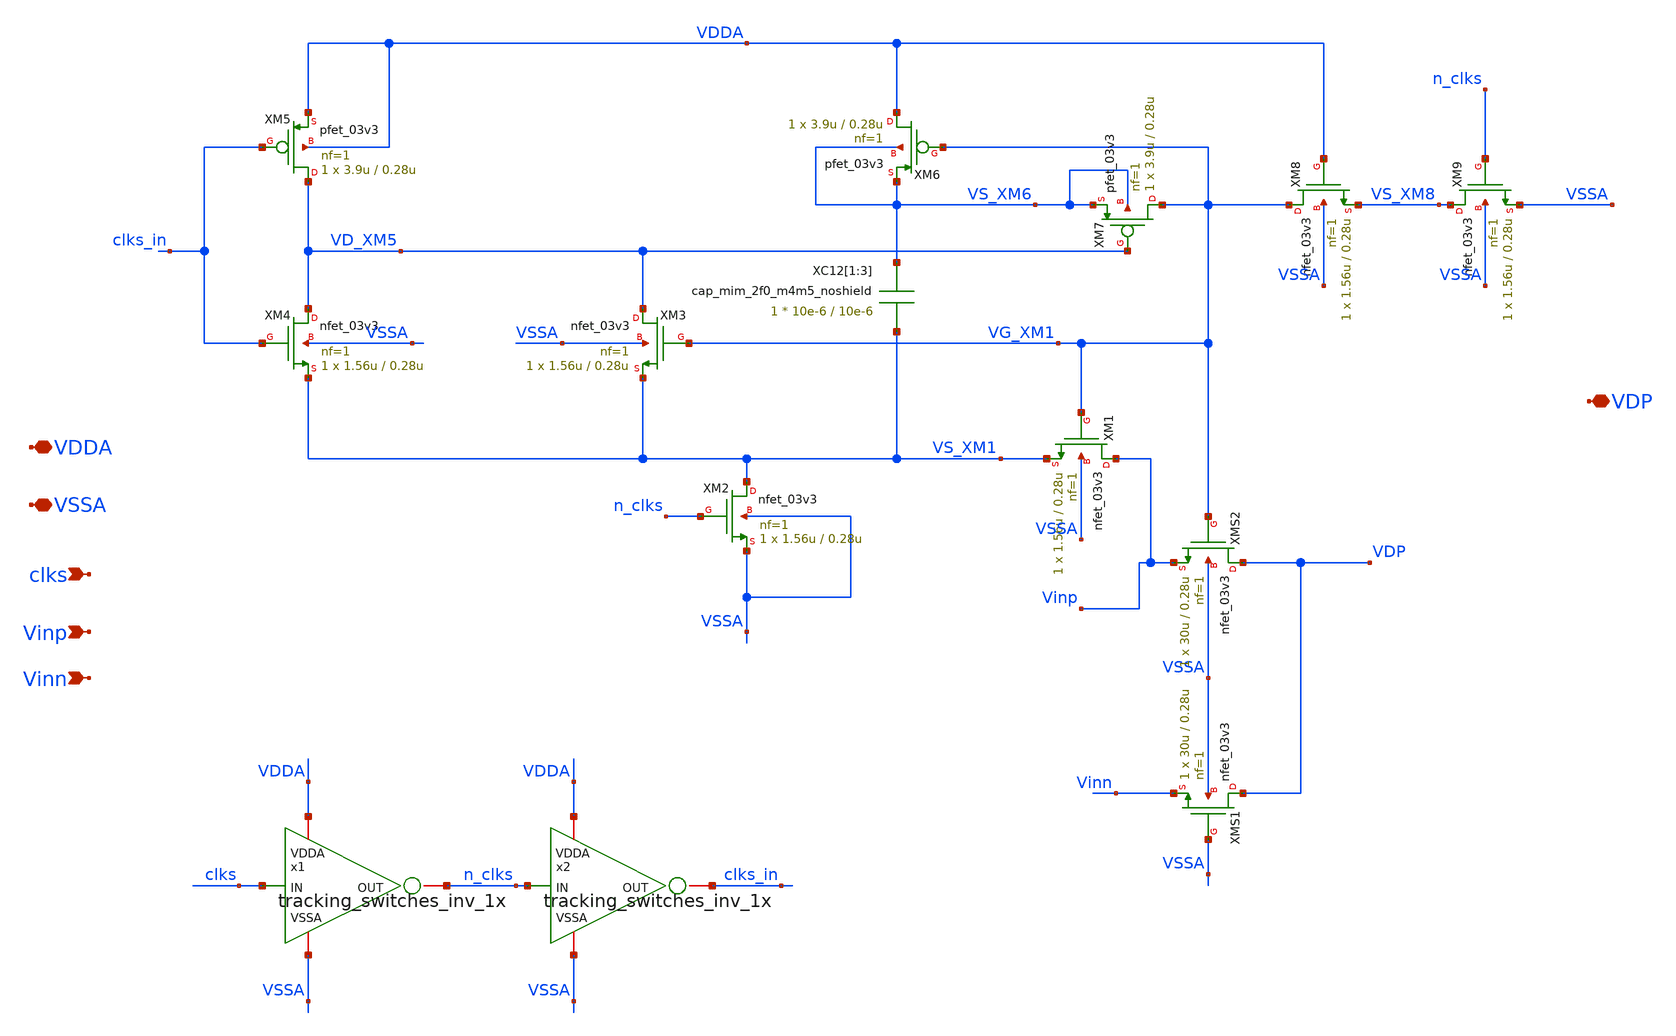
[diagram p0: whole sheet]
** sch_path: SAR_ADC/tracking_switches/xschem/tracking_switches_v1.sch
**.subckt tracking_switches_v1 VDDA VSSA clks Vinp VDP Vinn
*.iopin VDDA
*.iopin VSSA
*.ipin clks
*.ipin Vinp
*.iopin VDP
*.ipin Vinn
XM2 VS_XM1 n_clks VSSA VSSA nfet_03v3 L=0.28u W=1.56u nf=1 ad='int((nf+1)/2) * W/nf * 0.18u' as='int((nf+2)/2) * W/nf * 0.18u'
+ pd='2*int((nf+1)/2) * (W/nf + 0.18u)' ps='2*int((nf+2)/2) * (W/nf + 0.18u)' nrd='0.18u / W' nrs='0.18u / W'
+ sa=0 sb=0 sd=0 m=1
XM4 VD_XM5 clks_in VS_XM1 VSSA nfet_03v3 L=0.28u W=1.56u nf=1 ad='int((nf+1)/2) * W/nf * 0.18u' as='int((nf+2)/2) * W/nf * 0.18u'
+ pd='2*int((nf+1)/2) * (W/nf + 0.18u)' ps='2*int((nf+2)/2) * (W/nf + 0.18u)' nrd='0.18u / W' nrs='0.18u / W'
+ sa=0 sb=0 sd=0 m=1
XM3 VD_XM5 VG_XM1 VS_XM1 VSSA nfet_03v3 L=0.28u W=1.56u nf=1 ad='int((nf+1)/2) * W/nf * 0.18u' as='int((nf+2)/2) * W/nf * 0.18u'
+ pd='2*int((nf+1)/2) * (W/nf + 0.18u)' ps='2*int((nf+2)/2) * (W/nf + 0.18u)' nrd='0.18u / W' nrs='0.18u / W'
+ sa=0 sb=0 sd=0 m=1
XM5 VD_XM5 clks_in VDDA VDDA pfet_03v3 L=0.28u W=3.9u nf=1 ad='int((nf+1)/2) * W/nf * 0.18u' as='int((nf+2)/2) * W/nf * 0.18u'
+ pd='2*int((nf+1)/2) * (W/nf + 0.18u)' ps='2*int((nf+2)/2) * (W/nf + 0.18u)' nrd='0.18u / W' nrs='0.18u / W'
+ sa=0 sb=0 sd=0 m=1
XM6 VDDA VG_XM1 VS_XM6 VS_XM6 pfet_03v3 L=0.28u W=3.9u nf=1 ad='int((nf+1)/2) * W/nf * 0.18u' as='int((nf+2)/2) * W/nf * 0.18u'
+ pd='2*int((nf+1)/2) * (W/nf + 0.18u)' ps='2*int((nf+2)/2) * (W/nf + 0.18u)' nrd='0.18u / W' nrs='0.18u / W'
+ sa=0 sb=0 sd=0 m=1
XM7 VG_XM1 VD_XM5 VS_XM6 VS_XM6 pfet_03v3 L=0.28u W=3.9u nf=1 ad='int((nf+1)/2) * W/nf * 0.18u' as='int((nf+2)/2) * W/nf * 0.18u'
+ pd='2*int((nf+1)/2) * (W/nf + 0.18u)' ps='2*int((nf+2)/2) * (W/nf + 0.18u)' nrd='0.18u / W' nrs='0.18u / W'
+ sa=0 sb=0 sd=0 m=1
XM1 Vinp VG_XM1 VS_XM1 VSSA nfet_03v3 L=0.28u W=1.56u nf=1 ad='int((nf+1)/2) * W/nf * 0.18u' as='int((nf+2)/2) * W/nf * 0.18u'
+ pd='2*int((nf+1)/2) * (W/nf + 0.18u)' ps='2*int((nf+2)/2) * (W/nf + 0.18u)' nrd='0.18u / W' nrs='0.18u / W'
+ sa=0 sb=0 sd=0 m=1
XM9 VS_XM8 n_clks VSSA VSSA nfet_03v3 L=0.28u W=1.56u nf=1 ad='int((nf+1)/2) * W/nf * 0.18u' as='int((nf+2)/2) * W/nf * 0.18u'
+ pd='2*int((nf+1)/2) * (W/nf + 0.18u)' ps='2*int((nf+2)/2) * (W/nf + 0.18u)' nrd='0.18u / W' nrs='0.18u / W'
+ sa=0 sb=0 sd=0 m=1
XM8 VG_XM1 VDDA VS_XM8 VSSA nfet_03v3 L=0.28u W=1.56u nf=1 ad='int((nf+1)/2) * W/nf * 0.18u' as='int((nf+2)/2) * W/nf * 0.18u'
+ pd='2*int((nf+1)/2) * (W/nf + 0.18u)' ps='2*int((nf+2)/2) * (W/nf + 0.18u)' nrd='0.18u / W' nrs='0.18u / W'
+ sa=0 sb=0 sd=0 m=1
x1 VDDA VSSA n_clks clks tracking_switches_inv_1x
x2 VDDA VSSA clks_in n_clks tracking_switches_inv_1x
XMS2 VDP VG_XM1 Vinp VSSA nfet_03v3 L=0.28u W=30u nf=1 ad='int((nf+1)/2) * W/nf * 0.18u' as='int((nf+2)/2) * W/nf * 0.18u'
+ pd='2*int((nf+1)/2) * (W/nf + 0.18u)' ps='2*int((nf+2)/2) * (W/nf + 0.18u)' nrd='0.18u / W' nrs='0.18u / W'
+ sa=0 sb=0 sd=0 m=1
XC12[1] VS_XM6 VS_XM1 cap_mim_2f0_m4m5_noshield c_width=10e-6 c_length=10e-6 m=1
XC12[2] VS_XM6 VS_XM1 cap_mim_2f0_m4m5_noshield c_width=10e-6 c_length=10e-6 m=1
XC12[3] VS_XM6 VS_XM1 cap_mim_2f0_m4m5_noshield c_width=10e-6 c_length=10e-6 m=1
XMS1 VDP VSSA Vinn VSSA nfet_03v3 L=0.28u W=30u nf=1 ad='int((nf+1)/2) * W/nf * 0.18u' as='int((nf+2)/2) * W/nf * 0.18u'
+ pd='2*int((nf+1)/2) * (W/nf + 0.18u)' ps='2*int((nf+2)/2) * (W/nf + 0.18u)' nrd='0.18u / W' nrs='0.18u / W'
+ sa=0 sb=0 sd=0 m=1
**.ends

* expanding   symbol:  PICO_contest/tracking_switches/xschem/tracking_switches_inv_1x.sym # of
*+ pins=4
** sym_path: SAR_ADC/blocks/tracking_switches/tracking_switches_inv_1x.sym
** sch_path: SAR_ADC/blocks/tracking_switches/tracking_switches_inv_1x.sch
.subckt tracking_switches_inv_1x VDDA VSSA OUT IN
*.iopin VDDA
*.iopin VSSA
*.iopin OUT
*.ipin IN
XM1 OUT IN VSSA VSSA nfet_03v3 L=0.28u W=0.22u nf=1 ad='int((nf+1)/2) * W/nf * 0.18u' as='int((nf+2)/2) * W/nf * 0.18u'
+ pd='2*int((nf+1)/2) * (W/nf + 0.18u)' ps='2*int((nf+2)/2) * (W/nf + 0.18u)' nrd='0.18u / W' nrs='0.18u / W'
+ sa=0 sb=0 sd=0 m=1
XM2 OUT IN VDDA VDDA pfet_03v3 L=0.28u W=0.66u nf=1 ad='int((nf+1)/2) * W/nf * 0.18u' as='int((nf+2)/2) * W/nf * 0.18u'
+ pd='2*int((nf+1)/2) * (W/nf + 0.18u)' ps='2*int((nf+2)/2) * (W/nf + 0.18u)' nrd='0.18u / W' nrs='0.18u / W'
+ sa=0 sb=0 sd=0 m=1
.ends

.end
